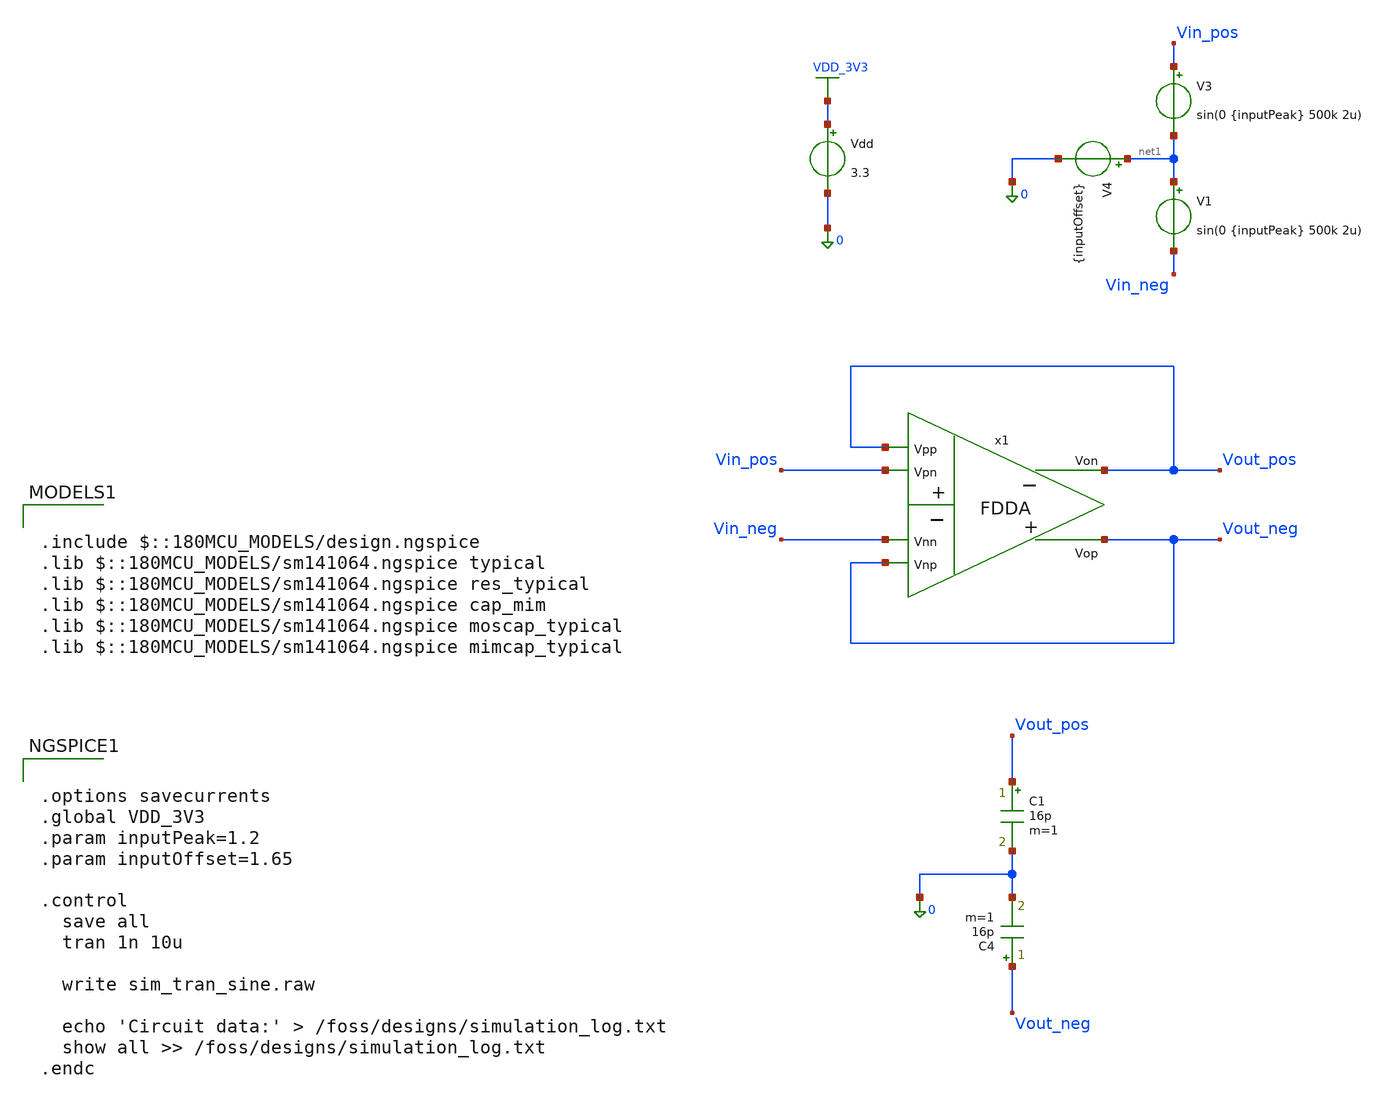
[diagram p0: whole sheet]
** sch_path: src/sim/sim_tran_sine.sch
**.subckt sim_tran_sine
Vdd VDD_3V3 0 3.3
.save i(vdd)
C1 Vout_pos 0 16p m=1
C4 Vout_neg 0 16p m=1
x1 Vout_pos Vout_neg Vout_neg Vin_neg Vout_pos Vin_pos fdda_subckt
V3 Vin_pos net1 sin(0 {inputPeak} 500k 2u)
.save i(v3)
V4 net1 0 {inputOffset}
.save i(v4)
V1 net1 Vin_neg sin(0 {inputPeak} 500k 2u)
.save i(v1)
**** begin user architecture code

.include $::180MCU_MODELS/design.ngspice
.lib $::180MCU_MODELS/sm141064.ngspice typical
.lib $::180MCU_MODELS/sm141064.ngspice res_typical
.lib $::180MCU_MODELS/sm141064.ngspice cap_mim
.lib $::180MCU_MODELS/sm141064.ngspice moscap_typical
.lib $::180MCU_MODELS/sm141064.ngspice mimcap_typical




.options savecurrents
.global VDD_3V3
.param inputPeak=1.2
.param inputOffset=1.65

.control
  save all
  tran 1n 10u

  write sim_tran_sine.raw

  echo 'Circuit data:' > /foss/designs/simulation_log.txt
  show all >> /foss/designs/simulation_log.txt
.endc


**** end user architecture code
**.ends
.GLOBAL VDD_3V3
.end
